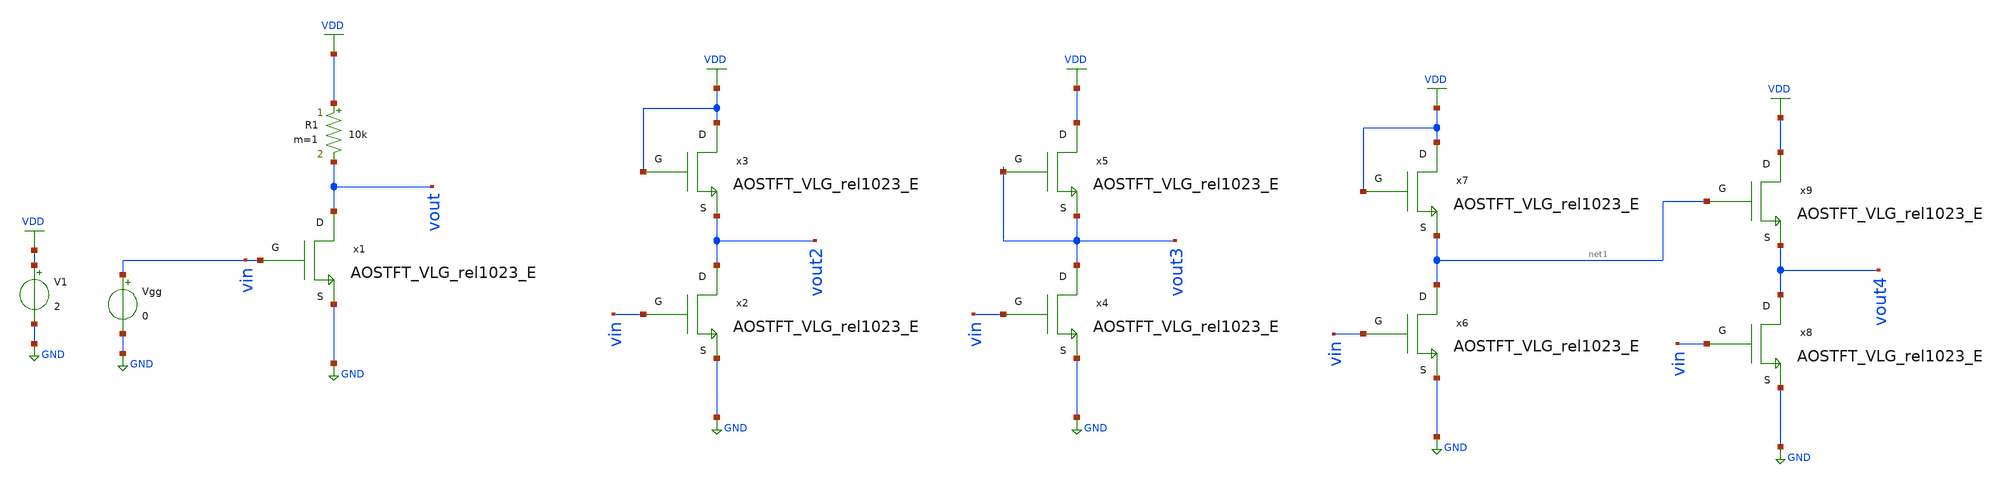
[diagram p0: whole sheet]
** sch_path: tb_inversores.sch
**.subckt tb_inversores
x1 vout vin GND AOSTFT_VLG_rel1023_E
R1 VDD vout 10k m=1
V1 VDD GND 2
Vgg vin GND 0
x2 vout2 vin GND AOSTFT_VLG_rel1023_E
x3 VDD VDD vout2 AOSTFT_VLG_rel1023_E
x4 vout3 vin GND AOSTFT_VLG_rel1023_E
x5 VDD vout3 vout3 AOSTFT_VLG_rel1023_E
x6 net1 vin GND AOSTFT_VLG_rel1023_E
x7 VDD VDD net1 AOSTFT_VLG_rel1023_E
x8 vout4 vin GND AOSTFT_VLG_rel1023_E
x9 VDD net1 vout4 AOSTFT_VLG_rel1023_E
**** begin user architecture code



.model VLG TFT TYPE =1				 TNOM		=27 L		=40e-6 W		=160e-6 TOX		=22e-9 TSI		=15e-9 TPAS		=400e-9
+ LOVDS		=5e-6 LOVTDS		=5e-6 EPS		=9 EPSI		=7 EPSPAS		=3.9 MU1		=8.98 VT0		=-2.27 GAMMA		=0.259 RS		=75 RD
+         	=75 ALPHAS		=0.727 M		=1.63 LAMBDA		=-0.0569 DELTA		=0 MUB1		=3.81 GAMMAB		=0.76 VFB		=-2.89 S		=0.237
+ V1A		=-1.793 V1		=-0.47 Q1		=33.7 V2		=1.11 Q2		=0.66 I0		=5E-13 VDSlin		=0.1 V3		=0 Q3		=0 ALPHASS	=0
+ CGGDEP		=4.1e-12 CGGACU		=19.6e-12 MM		=0.0 a		=0.00 DD		=0.0 VAC		=0. capmod 	=param_capmod




.param param_capmod = 1

.subckt AOSTFT_VLG_rel1023_E D G S
	N1 D G S VLG
.ends AOSTFT_VLG_rel1023_E


.dc vgg   0   3   0.1
.control
	pre_osdi /home/alex/Desktop/EDA/MALEMAN/AOSTFT_VLG_rel1023_E.osdi
	run
	setplot dc1
	plot vout vout2 vout3 vout4
.endc


**** end user architecture code
**.ends
.GLOBAL GND
.GLOBAL VDD
.end
